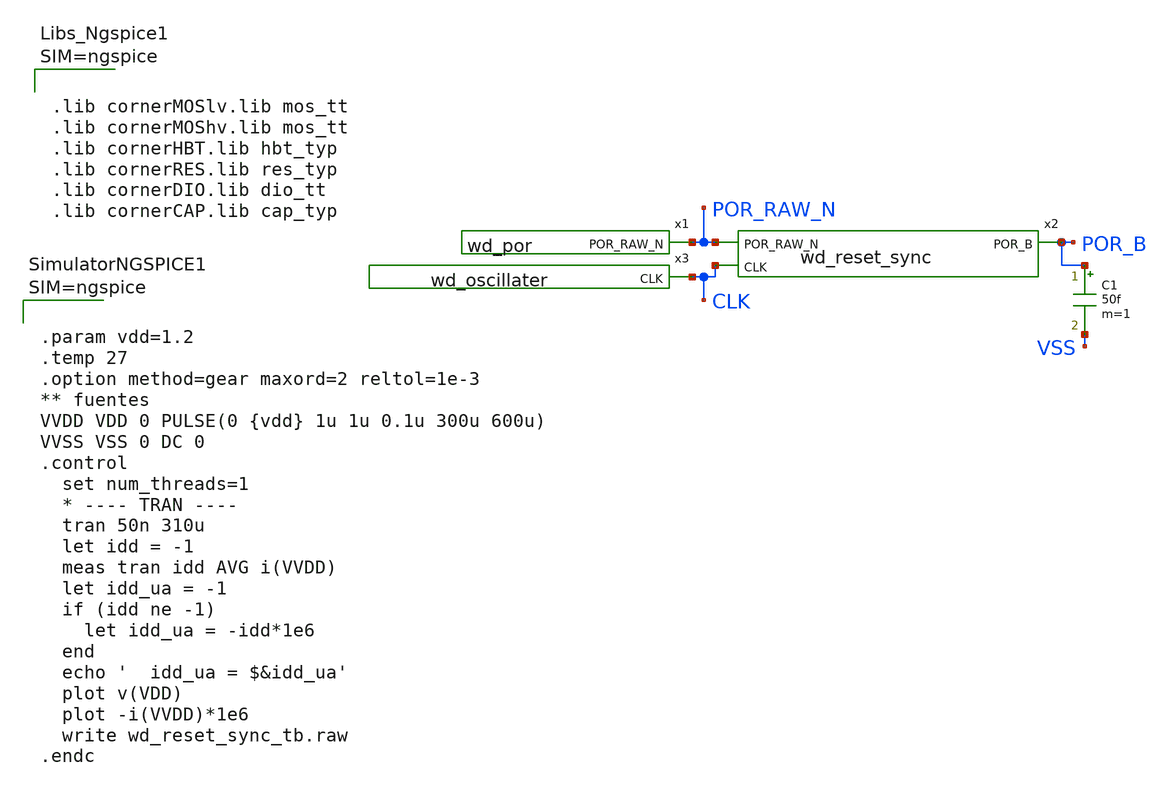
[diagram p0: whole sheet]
** sch_path: design/blocks/por/schematic/wd_reset_sync_tb.sch
**.subckt wd_reset_sync_tb
x1 POR_RAW_N VDD VSS wd_por
x2 POR_RAW_N CLK POR_B VDD VSS wd_reset_sync
x3 CLK VDD VSS wd_oscillater
C1 POR_B VSS 50f m=1
**** begin user architecture code



.lib cornerMOSlv.lib mos_tt
.lib cornerMOShv.lib mos_tt
.lib cornerHBT.lib hbt_typ
.lib cornerRES.lib res_typ
.lib cornerDIO.lib dio_tt
.lib cornerCAP.lib cap_typ






.param vdd=1.2
.temp 27
.option method=gear maxord=2 reltol=1e-3
** fuentes
VVDD VDD 0 PULSE(0 {vdd} 1u 1u 0.1u 300u 600u)
VVSS VSS 0 DC 0
.control
  set num_threads=1
  * ---- TRAN ----
  tran 50n 310u
  let idd = -1
  meas tran idd AVG i(VVDD)
  let idd_ua = -1
  if (idd ne -1)
    let idd_ua = -idd*1e6
  end
  echo '  idd_ua = $&idd_ua'
  plot v(VDD)
  plot -i(VVDD)*1e6
  write wd_reset_sync_tb.raw
.endc



**** end user architecture code
**.ends
.end
